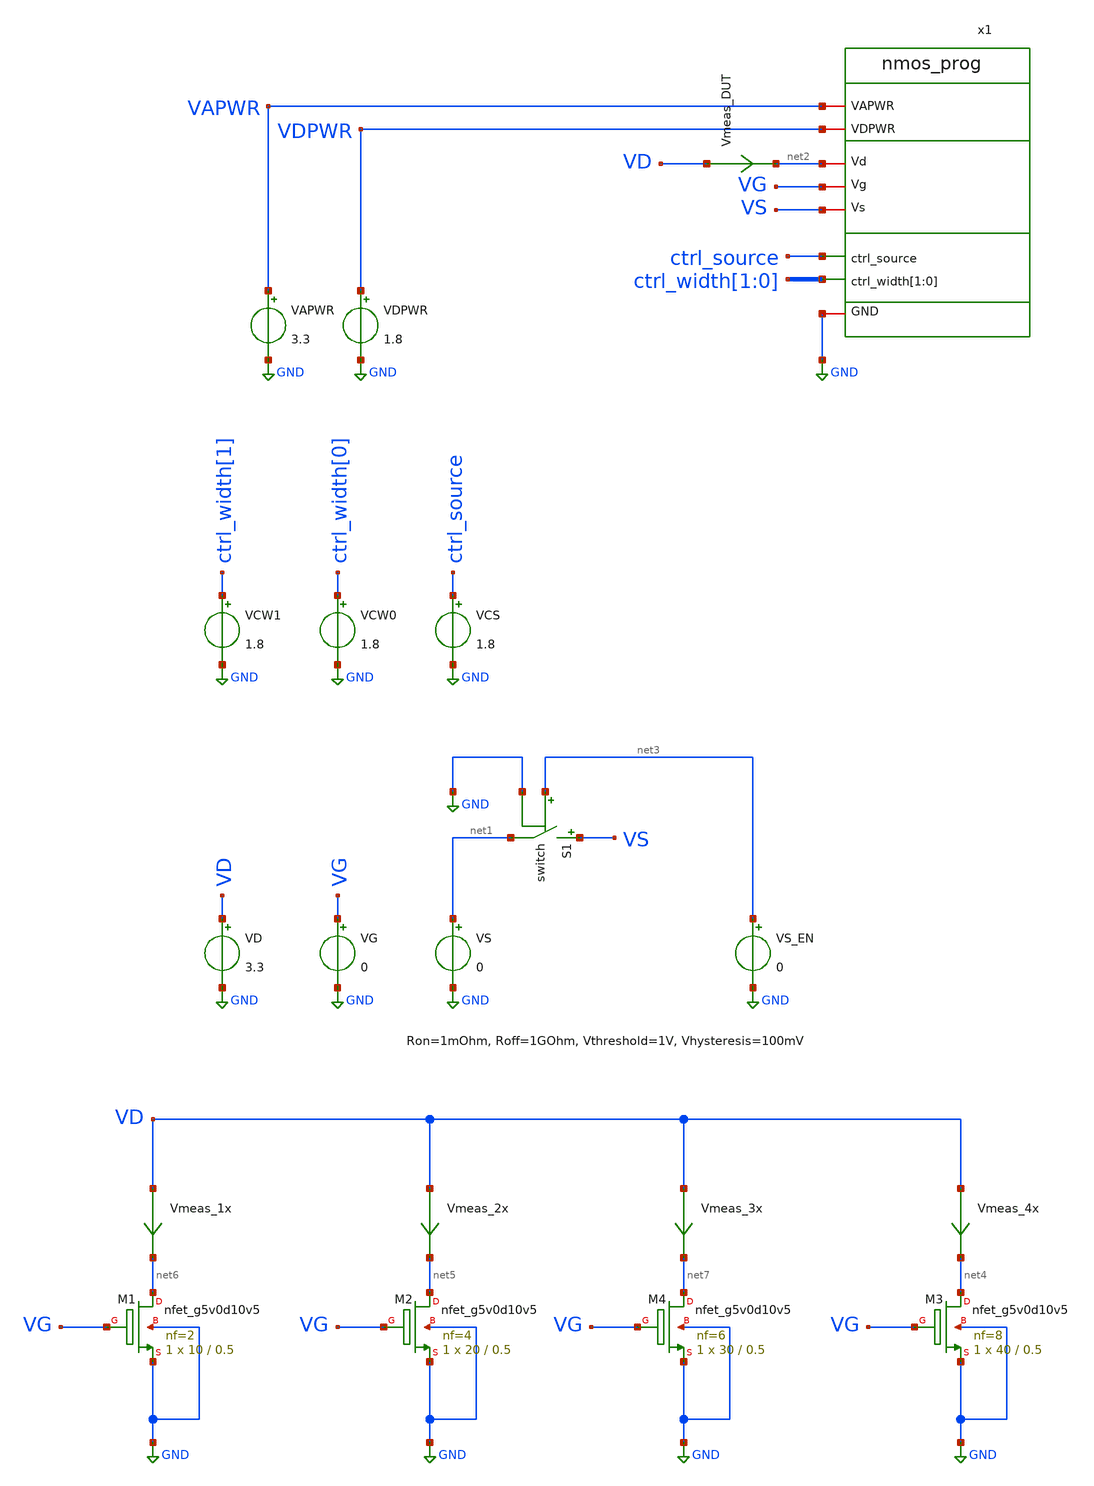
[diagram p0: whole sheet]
** sch_path: xschem/tb_nmos_prog.sch
**.subckt tb_nmos_prog
x1 VAPWR VDPWR net2 VG VS ctrl_source ctrl_width[1] ctrl_width[0] GND nmos_prog
VAPWR VAPWR GND 3.3
VDPWR VDPWR GND 1.8
VCW1 ctrl_width[1] GND 1.8
VCW0 ctrl_width[0] GND 1.8
VCS ctrl_source GND 1.8
VD VD GND 3.3
VG VG GND 0
VS net1 GND 0
VS_EN net3 GND 0
S1 VS net1 net3 GND switch
XM1 net6 VG GND GND sky130_fd_pr__nfet_g5v0d10v5 L=0.5 W=10 nf=2 ad='int((nf+1)/2) * W/nf * 0.29' as='int((nf+2)/2) * W/nf * 0.29'
+ pd='2*int((nf+1)/2) * (W/nf + 0.29)' ps='2*int((nf+2)/2) * (W/nf + 0.29)' nrd='0.29 / W' nrs='0.29 / W'
+ sa=0 sb=0 sd=0 mult=1 m=1
XM2 net5 VG GND GND sky130_fd_pr__nfet_g5v0d10v5 L=0.5 W=20 nf=4 ad='int((nf+1)/2) * W/nf * 0.29' as='int((nf+2)/2) * W/nf * 0.29'
+ pd='2*int((nf+1)/2) * (W/nf + 0.29)' ps='2*int((nf+2)/2) * (W/nf + 0.29)' nrd='0.29 / W' nrs='0.29 / W'
+ sa=0 sb=0 sd=0 mult=1 m=1
XM3 net4 VG GND GND sky130_fd_pr__nfet_g5v0d10v5 L=0.5 W=40 nf=8 ad='int((nf+1)/2) * W/nf * 0.29' as='int((nf+2)/2) * W/nf * 0.29'
+ pd='2*int((nf+1)/2) * (W/nf + 0.29)' ps='2*int((nf+2)/2) * (W/nf + 0.29)' nrd='0.29 / W' nrs='0.29 / W'
+ sa=0 sb=0 sd=0 mult=1 m=1
Vmeas_1x VD net6 0
.save i(vmeas_1x)
Vmeas_DUT VD net2 0
.save i(vmeas_dut)
Vmeas_2x VD net5 0
.save i(vmeas_2x)
Vmeas_4x VD net4 0
.save i(vmeas_4x)
XM4 net7 VG GND GND sky130_fd_pr__nfet_g5v0d10v5 L=0.5 W=30 nf=6 ad='int((nf+1)/2) * W/nf * 0.29' as='int((nf+2)/2) * W/nf * 0.29'
+ pd='2*int((nf+1)/2) * (W/nf + 0.29)' ps='2*int((nf+2)/2) * (W/nf + 0.29)' nrd='0.29 / W' nrs='0.29 / W'
+ sa=0 sb=0 sd=0 mult=1 m=1
Vmeas_3x VD net7 0
.save i(vmeas_3x)
**** begin user architecture code
.lib $::SKYWATER_MODELS/sky130.lib.spice tt


*****************************************
* VGS Sweep Test
*****************************************
* this test does a ID vs VGS DC sweep for a common source configuration
* and plots the current vs ideal NMOS devices.
* plots 1-4 represent each programmed NMOS width
*****************************************
.model switch SW(Ron=1m, Roff=1G, Vt=0.5, Vh=0.1)
.control
   save all
   set temp = 27
   set wr_singlescale
   set wr_vecnames
   alter VD 3.3
   alter VCW1 0
   alter VCW0 0
   alter VCS 1.8
   alter VS_EN 0
   repeat 2
      repeat 2
         dc VG 0 3.3 0.01
         alter VCW0 1.8
      end
      alter VCW1 1.8
      alter VCW0 0
   end
   plot dc1.i(Vmeas_DUT) dc1.i(Vmeas_1x); ylog
   plot dc2.i(Vmeas_DUT) dc2.i(Vmeas_2x); ylog
   plot dc3.i(Vmeas_DUT) dc3.i(Vmeas_3x); ylog
   plot dc4.i(Vmeas_DUT) dc4.i(Vmeas_4x); ylog
.endc


**** end user architecture code
**.ends
.GLOBAL GND
.end
